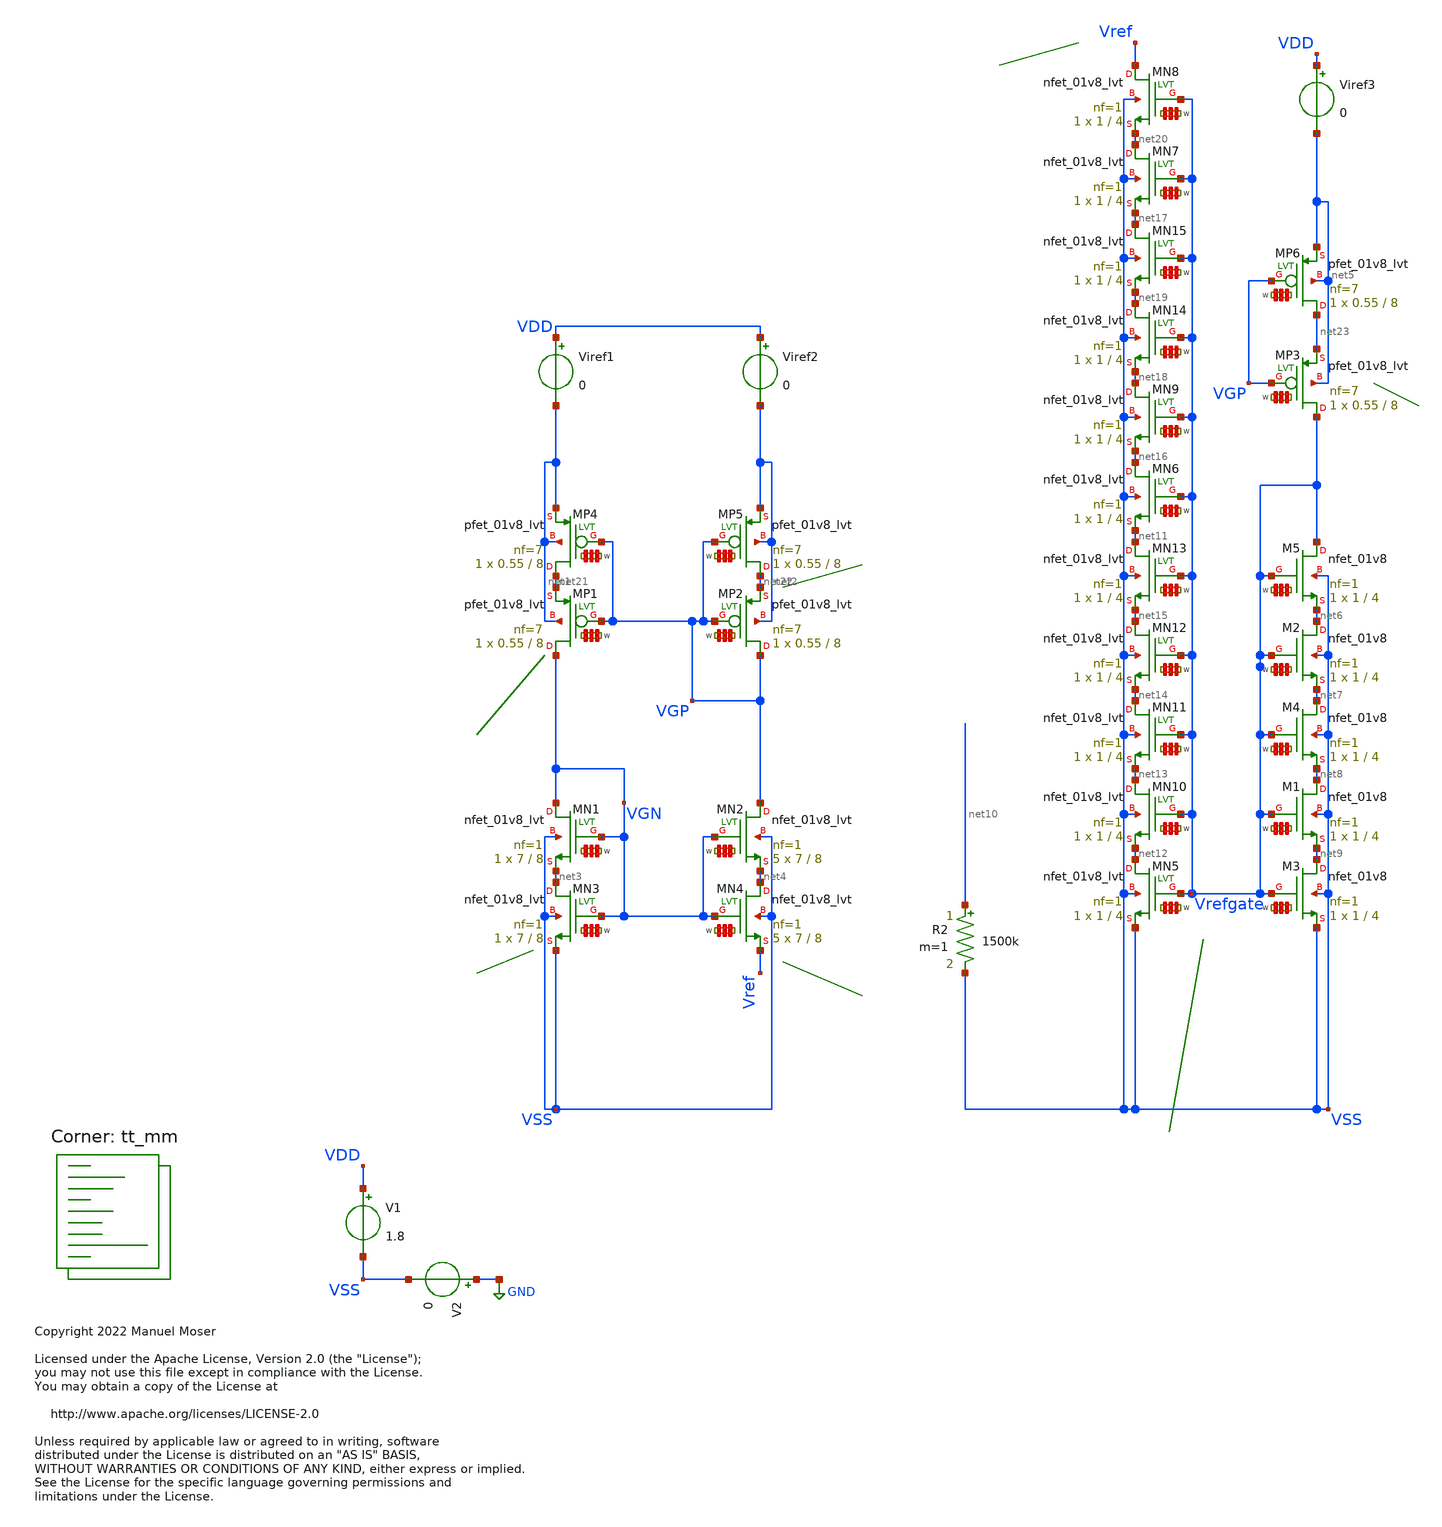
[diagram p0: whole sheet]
** sch_path: xschem/ldo_isource_eval.sch
* Copyright 2022 Manuel Moser
* Licensed under the Apache License, Version 2.0 (the "License");
**.subckt ldo_isource_eval
V1 VDD VSS 1.8
V2 GND VSS 0
XMP2 VGP VGP net22 net2 sky130_fd_pr__pfet_01v8_lvt L=8 W='0.55 * 7 ' nf=7 ad='int((nf+1)/2) * W / nf * 0.29'
+ as='int((nf+2)/2) * W / nf * 0.29' pd='2*int((nf+1)/2) * (W / nf + 0.29)' ps='2*int((nf+2)/2) * (W / nf + 0.29)'
+ nrd='0.29 / W ' nrs='0.29 / W ' sa=0 sb=0 sd=0 mult=1 m=1
XMP1 VGN VGP net21 net1 sky130_fd_pr__pfet_01v8_lvt L=8 W='0.55 * 7 ' nf=7 ad='int((nf+1)/2) * W / nf * 0.29'
+ as='int((nf+2)/2) * W / nf * 0.29' pd='2*int((nf+1)/2) * (W / nf + 0.29)' ps='2*int((nf+2)/2) * (W / nf + 0.29)'
+ nrd='0.29 / W ' nrs='0.29 / W ' sa=0 sb=0 sd=0 mult=1 m=1
XMN1 VGN VGN net3 VSS sky130_fd_pr__nfet_01v8_lvt L=8 W='7 * 1 ' nf=1 ad='int((nf+1)/2) * W / nf * 0.29'
+ as='int((nf+2)/2) * W / nf * 0.29' pd='2*int((nf+1)/2) * (W / nf + 0.29)' ps='2*int((nf+2)/2) * (W / nf + 0.29)'
+ nrd='0.29 / W ' nrs='0.29 / W ' sa=0 sb=0 sd=0 mult=1 m=1
XMN2 VGP VGN net4 VSS sky130_fd_pr__nfet_01v8_lvt L=8 W='7 * 1 ' nf=1 ad='int((nf+1)/2) * W / nf * 0.29'
+ as='int((nf+2)/2) * W / nf * 0.29' pd='2*int((nf+1)/2) * (W / nf + 0.29)' ps='2*int((nf+2)/2) * (W / nf + 0.29)'
+ nrd='0.29 / W ' nrs='0.29 / W ' sa=0 sb=0 sd=0 mult=5 m=5
Viref1 VDD net1 0
Viref2 VDD net2 0
XMN3 net3 VGN VSS VSS sky130_fd_pr__nfet_01v8_lvt L=8 W='7 * 1 ' nf=1 ad='int((nf+1)/2) * W / nf * 0.29'
+ as='int((nf+2)/2) * W / nf * 0.29' pd='2*int((nf+1)/2) * (W / nf + 0.29)' ps='2*int((nf+2)/2) * (W / nf + 0.29)'
+ nrd='0.29 / W ' nrs='0.29 / W ' sa=0 sb=0 sd=0 mult=1 m=1
XMN4 net4 VGN Vref VSS sky130_fd_pr__nfet_01v8_lvt L=8 W='7 * 1 ' nf=1 ad='int((nf+1)/2) * W / nf * 0.29'
+ as='int((nf+2)/2) * W / nf * 0.29' pd='2*int((nf+1)/2) * (W / nf + 0.29)' ps='2*int((nf+2)/2) * (W / nf + 0.29)'
+ nrd='0.29 / W ' nrs='0.29 / W ' sa=0 sb=0 sd=0 mult=5 m=5
XMP3 Vrefgate VGP net23 net5 sky130_fd_pr__pfet_01v8_lvt L=8 W='0.55 * 7 ' nf=7 ad='int((nf+1)/2) * W / nf * 0.29'
+ as='int((nf+2)/2) * W / nf * 0.29' pd='2*int((nf+1)/2) * (W / nf + 0.29)' ps='2*int((nf+2)/2) * (W / nf + 0.29)'
+ nrd='0.29 / W ' nrs='0.29 / W ' sa=0 sb=0 sd=0 mult=1 m=1
Viref3 VDD net5 0
XM2 net6 Vrefgate net7 VSS sky130_fd_pr__nfet_01v8 L=4 W='1 * 1 ' nf=1 ad='int((nf+1)/2) * W / nf * 0.29'
+ as='int((nf+2)/2) * W / nf * 0.29' pd='2*int((nf+1)/2) * (W / nf + 0.29)' ps='2*int((nf+2)/2) * (W / nf + 0.29)'
+ nrd='0.29 / W ' nrs='0.29 / W ' sa=0 sb=0 sd=0 mult=1 m=1
XM3 net9 Vrefgate VSS VSS sky130_fd_pr__nfet_01v8 L=4 W='1 * 1 ' nf=1 ad='int((nf+1)/2) * W / nf * 0.29'
+ as='int((nf+2)/2) * W / nf * 0.29' pd='2*int((nf+1)/2) * (W / nf + 0.29)' ps='2*int((nf+2)/2) * (W / nf + 0.29)'
+ nrd='0.29 / W ' nrs='0.29 / W ' sa=0 sb=0 sd=0 mult=1 m=1
XM1 net8 Vrefgate net9 VSS sky130_fd_pr__nfet_01v8 L=4 W='1 * 1 ' nf=1 ad='int((nf+1)/2) * W / nf * 0.29'
+ as='int((nf+2)/2) * W / nf * 0.29' pd='2*int((nf+1)/2) * (W / nf + 0.29)' ps='2*int((nf+2)/2) * (W / nf + 0.29)'
+ nrd='0.29 / W ' nrs='0.29 / W ' sa=0 sb=0 sd=0 mult=1 m=1
XM4 net7 Vrefgate net8 VSS sky130_fd_pr__nfet_01v8 L=4 W='1 * 1 ' nf=1 ad='int((nf+1)/2) * W / nf * 0.29'
+ as='int((nf+2)/2) * W / nf * 0.29' pd='2*int((nf+1)/2) * (W / nf + 0.29)' ps='2*int((nf+2)/2) * (W / nf + 0.29)'
+ nrd='0.29 / W ' nrs='0.29 / W ' sa=0 sb=0 sd=0 mult=1 m=1
XMN5 net12 Vrefgate VSS VSS sky130_fd_pr__nfet_01v8_lvt L=4 W='1 * 1 ' nf=1 ad='int((nf+1)/2) * W / nf * 0.29'
+ as='int((nf+2)/2) * W / nf * 0.29' pd='2*int((nf+1)/2) * (W / nf + 0.29)' ps='2*int((nf+2)/2) * (W / nf + 0.29)'
+ nrd='0.29 / W ' nrs='0.29 / W ' sa=0 sb=0 sd=0 mult=1 m=1
XMN6 net16 Vrefgate net11 VSS sky130_fd_pr__nfet_01v8_lvt L=4 W='1 * 1 ' nf=1 ad='int((nf+1)/2) * W / nf * 0.29'
+ as='int((nf+2)/2) * W / nf * 0.29' pd='2*int((nf+1)/2) * (W / nf + 0.29)' ps='2*int((nf+2)/2) * (W / nf + 0.29)'
+ nrd='0.29 / W ' nrs='0.29 / W ' sa=0 sb=0 sd=0 mult=1 m=1
XMN9 net18 Vrefgate net16 VSS sky130_fd_pr__nfet_01v8_lvt L=4 W='1 * 1 ' nf=1 ad='int((nf+1)/2) * W / nf * 0.29'
+ as='int((nf+2)/2) * W / nf * 0.29' pd='2*int((nf+1)/2) * (W / nf + 0.29)' ps='2*int((nf+2)/2) * (W / nf + 0.29)'
+ nrd='0.29 / W ' nrs='0.29 / W ' sa=0 sb=0 sd=0 mult=1 m=1
XM5 Vrefgate Vrefgate net6 VSS sky130_fd_pr__nfet_01v8 L=4 W='1 * 1 ' nf=1 ad='int((nf+1)/2) * W / nf * 0.29'
+ as='int((nf+2)/2) * W / nf * 0.29' pd='2*int((nf+1)/2) * (W / nf + 0.29)' ps='2*int((nf+2)/2) * (W / nf + 0.29)'
+ nrd='0.29 / W ' nrs='0.29 / W ' sa=0 sb=0 sd=0 mult=1 m=1
XMN10 net13 Vrefgate net12 VSS sky130_fd_pr__nfet_01v8_lvt L=4 W='1 * 1 ' nf=1 ad='int((nf+1)/2) * W / nf * 0.29'
+ as='int((nf+2)/2) * W / nf * 0.29' pd='2*int((nf+1)/2) * (W / nf + 0.29)' ps='2*int((nf+2)/2) * (W / nf + 0.29)'
+ nrd='0.29 / W ' nrs='0.29 / W ' sa=0 sb=0 sd=0 mult=1 m=1
XMN11 net14 Vrefgate net13 VSS sky130_fd_pr__nfet_01v8_lvt L=4 W='1 * 1 ' nf=1 ad='int((nf+1)/2) * W / nf * 0.29'
+ as='int((nf+2)/2) * W / nf * 0.29' pd='2*int((nf+1)/2) * (W / nf + 0.29)' ps='2*int((nf+2)/2) * (W / nf + 0.29)'
+ nrd='0.29 / W ' nrs='0.29 / W ' sa=0 sb=0 sd=0 mult=1 m=1
XMN12 net15 Vrefgate net14 VSS sky130_fd_pr__nfet_01v8_lvt L=4 W='1 * 1 ' nf=1 ad='int((nf+1)/2) * W / nf * 0.29'
+ as='int((nf+2)/2) * W / nf * 0.29' pd='2*int((nf+1)/2) * (W / nf + 0.29)' ps='2*int((nf+2)/2) * (W / nf + 0.29)'
+ nrd='0.29 / W ' nrs='0.29 / W ' sa=0 sb=0 sd=0 mult=1 m=1
XMN13 net11 Vrefgate net15 VSS sky130_fd_pr__nfet_01v8_lvt L=4 W='1 * 1 ' nf=1 ad='int((nf+1)/2) * W / nf * 0.29'
+ as='int((nf+2)/2) * W / nf * 0.29' pd='2*int((nf+1)/2) * (W / nf + 0.29)' ps='2*int((nf+2)/2) * (W / nf + 0.29)'
+ nrd='0.29 / W ' nrs='0.29 / W ' sa=0 sb=0 sd=0 mult=1 m=1
XMN7 net20 Vrefgate net17 VSS sky130_fd_pr__nfet_01v8_lvt L=4 W='1 * 1 ' nf=1 ad='int((nf+1)/2) * W / nf * 0.29'
+ as='int((nf+2)/2) * W / nf * 0.29' pd='2*int((nf+1)/2) * (W / nf + 0.29)' ps='2*int((nf+2)/2) * (W / nf + 0.29)'
+ nrd='0.29 / W ' nrs='0.29 / W ' sa=0 sb=0 sd=0 mult=1 m=1
XMN8 Vref Vrefgate net20 VSS sky130_fd_pr__nfet_01v8_lvt L=4 W='1 * 1 ' nf=1 ad='int((nf+1)/2) * W / nf * 0.29'
+ as='int((nf+2)/2) * W / nf * 0.29' pd='2*int((nf+1)/2) * (W / nf + 0.29)' ps='2*int((nf+2)/2) * (W / nf + 0.29)'
+ nrd='0.29 / W ' nrs='0.29 / W ' sa=0 sb=0 sd=0 mult=1 m=1
XMN14 net19 Vrefgate net18 VSS sky130_fd_pr__nfet_01v8_lvt L=4 W='1 * 1 ' nf=1 ad='int((nf+1)/2) * W / nf * 0.29'
+ as='int((nf+2)/2) * W / nf * 0.29' pd='2*int((nf+1)/2) * (W / nf + 0.29)' ps='2*int((nf+2)/2) * (W / nf + 0.29)'
+ nrd='0.29 / W ' nrs='0.29 / W ' sa=0 sb=0 sd=0 mult=1 m=1
XMN15 net17 Vrefgate net19 VSS sky130_fd_pr__nfet_01v8_lvt L=4 W='1 * 1 ' nf=1 ad='int((nf+1)/2) * W / nf * 0.29'
+ as='int((nf+2)/2) * W / nf * 0.29' pd='2*int((nf+1)/2) * (W / nf + 0.29)' ps='2*int((nf+2)/2) * (W / nf + 0.29)'
+ nrd='0.29 / W ' nrs='0.29 / W ' sa=0 sb=0 sd=0 mult=1 m=1
R2 net10 VSS 1500k m=1
XMP4 net21 VGP net1 net1 sky130_fd_pr__pfet_01v8_lvt L=8 W='0.55 * 7 ' nf=7 ad='int((nf+1)/2) * W / nf * 0.29'
+ as='int((nf+2)/2) * W / nf * 0.29' pd='2*int((nf+1)/2) * (W / nf + 0.29)' ps='2*int((nf+2)/2) * (W / nf + 0.29)'
+ nrd='0.29 / W ' nrs='0.29 / W ' sa=0 sb=0 sd=0 mult=1 m=1
XMP5 net22 VGP net2 net2 sky130_fd_pr__pfet_01v8_lvt L=8 W='0.55 * 7 ' nf=7 ad='int((nf+1)/2) * W / nf * 0.29'
+ as='int((nf+2)/2) * W / nf * 0.29' pd='2*int((nf+1)/2) * (W / nf + 0.29)' ps='2*int((nf+2)/2) * (W / nf + 0.29)'
+ nrd='0.29 / W ' nrs='0.29 / W ' sa=0 sb=0 sd=0 mult=1 m=1
XMP6 net23 VGP net5 net5 sky130_fd_pr__pfet_01v8_lvt L=8 W='0.55 * 7 ' nf=7 ad='int((nf+1)/2) * W / nf * 0.29'
+ as='int((nf+2)/2) * W / nf * 0.29' pd='2*int((nf+1)/2) * (W / nf + 0.29)' ps='2*int((nf+2)/2) * (W / nf + 0.29)'
+ nrd='0.29 / W ' nrs='0.29 / W ' sa=0 sb=0 sd=0 mult=1 m=1
**** begin user architecture code



.temp 27
.options savecurrents
.save all

* Save NMOS
.save @m.xmn1.msky130_fd_pr__nfet_01v8_lvt[Vth] @m.xmn1.msky130_fd_pr__nfet_01v8_lvt[Vgs] @m.xmn1.msky130_fd_pr__nfet_01v8_lvt[Vds]
.save @m.xmn2.msky130_fd_pr__nfet_01v8_lvt[Vth] @m.xmn2.msky130_fd_pr__nfet_01v8_lvt[Vgs] @m.xmn2.msky130_fd_pr__nfet_01v8_lvt[Vds]

* Save PMOS
.save @m.xmp1.msky130_fd_pr__pfet_01v8_lvt[Vth] @m.xmp1.msky130_fd_pr__pfet_01v8_lvt[Vgs] @m.xmp1.msky130_fd_pr__pfet_01v8_lvt[Vds]
.save @m.xmp2.msky130_fd_pr__pfet_01v8_lvt[Vth] @m.xmp2.msky130_fd_pr__pfet_01v8_lvt[Vgs] @m.xmp2.msky130_fd_pr__pfet_01v8_lvt[Vds]
.save @m.xmp3.msky130_fd_pr__pfet_01v8_lvt[Vth] @m.xmp3.msky130_fd_pr__pfet_01v8_lvt[Vgs] @m.xmp3.msky130_fd_pr__pfet_01v8_lvt[Vds]

* currents
.save i(Viref1) i(Viref2)

.op

.control
set num_threads = 12
write results.raw
set appendwrite

repeat 40
  reset
  *dc V1 0 2 0.02
  dc V1 0 2 0.02 temp -30 60 90
  *dc temp -30 60 1

  * NMOS
  let MN1_vov =
+ (v(@m.xmn1.msky130_fd_pr__nfet_01v8_lvt[Vgs])-v(@m.xmn1.msky130_fd_pr__nfet_01v8_lvt[Vth]))
  let MN2_vov =
+ (v(@m.xmn2.msky130_fd_pr__nfet_01v8_lvt[Vgs])-v(@m.xmn2.msky130_fd_pr__nfet_01v8_lvt[Vth]))
  let MN1_vsat =(v(@m.xmn1.msky130_fd_pr__nfet_01v8_lvt[VDS])-MN1_vov)
  let MN2_vsat =(v(@m.xmn2.msky130_fd_pr__nfet_01v8_lvt[VDS])-MN2_vov)

  * PMOS
  let MP1_vov =
+ (v(@m.xmp1.msky130_fd_pr__pfet_01v8_lvt[Vgs])-v(@m.xmp1.msky130_fd_pr__pfet_01v8_lvt[Vth]))
  let MP2_vov =
+ (v(@m.xmp2.msky130_fd_pr__pfet_01v8_lvt[Vgs])-v(@m.xmp2.msky130_fd_pr__pfet_01v8_lvt[Vth]))
  let MP3_vov =
+ (v(@m.xmp3.msky130_fd_pr__pfet_01v8_lvt[Vgs])-v(@m.xmp3.msky130_fd_pr__pfet_01v8_lvt[Vth]))
  let MP1_vsat = (v(@m.xmp1.msky130_fd_pr__pfet_01v8_lvt[VDS])-MP1_vov)
  let MP2_vsat = (v(@m.xmp2.msky130_fd_pr__pfet_01v8_lvt[VDS])-MP2_vov)
  let MP3_vsat = (v(@m.xmp3.msky130_fd_pr__pfet_01v8_lvt[VDS])-MP3_vov)
  write results.raw MN1_vov MN2_vov MN1_vsat MN2_vsat MP1_vov MP2_vov MP3_vov MP1_vsat MP2_vsat
+ MP3_vsat vref vrefgate i(Viref1) i(Viref2)
end

.endc




.lib $::SKYWATER_MODELS/sky130.lib.spice tt_mm
**** end user architecture code
**.ends
.GLOBAL GND
.end
